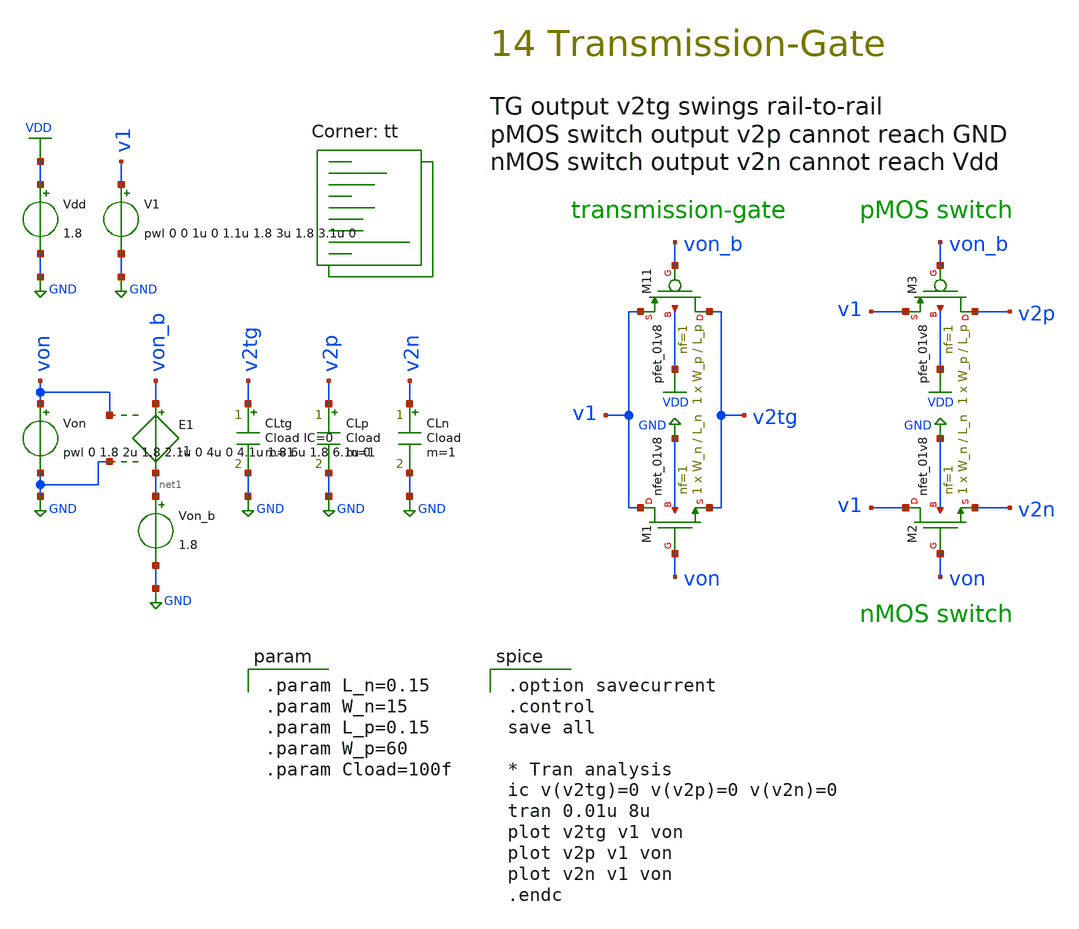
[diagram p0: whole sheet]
** sch_path: 14-b_transmission-gate_tran.sch
**.subckt 14-b_transmission-gate_tran
XM1 v1 von v2tg GND sky130_fd_pr__nfet_01v8 L=L_n W=W_n nf=1 ad='int((1 + 1)/2) * W_n / 1 * 0.29' as='int((1 + 2)/2) * W_n / 1 * 0.29'
+ pd='2*int((1 + 1)/2) * (W_n / 1 + 0.29)' ps='2*int((1 + 2)/2) * (W_n / 1 + 0.29)' nrd='0.29 / W_n ' nrs='0.29 / W_n '
+ sa=0 sb=0 sd=0 mult=1 m=1
V1 v1 GND pwl 0 0 1u 0 1.1u 1.8 3u 1.8 3.1u 0
Von von GND pwl 0 1.8 2u 1.8 2.1u 0 4u 0 4.1u 1.8 6u 1.8 6.1u 0
E1 von_b net1 von GND -1
Von_b net1 GND 1.8
XM11 v2tg von_b v1 VDD sky130_fd_pr__pfet_01v8 L=L_p W=W_p nf=1 ad='int((nf+1)/2) * W/nf * 0.29' as='int((nf+2)/2) * W/nf * 0.29'
+ pd='2*int((nf+1)/2) * (W/nf + 0.29)' ps='2*int((nf+2)/2) * (W/nf + 0.29)' nrd='0.29 / W' nrs='0.29 / W'
+ sa=0 sb=0 sd=0 mult=1 m=1
Vdd VDD GND 1.8
CLtg v2tg GND Cload IC=0 m=1
CLp v2p GND Cload m=1
CLn v2n GND Cload m=1
XM2 v1 von v2n GND sky130_fd_pr__nfet_01v8 L=L_n W=W_n nf=1 ad='int((1 + 1)/2) * W_n / 1 * 0.29' as='int((1 + 2)/2) * W_n / 1 * 0.29'
+ pd='2*int((1 + 1)/2) * (W_n / 1 + 0.29)' ps='2*int((1 + 2)/2) * (W_n / 1 + 0.29)' nrd='0.29 / W_n ' nrs='0.29 / W_n '
+ sa=0 sb=0 sd=0 mult=1 m=1
XM3 v2p von_b v1 VDD sky130_fd_pr__pfet_01v8 L=L_p W=W_p nf=1 ad='int((nf+1)/2) * W/nf * 0.29' as='int((nf+2)/2) * W/nf * 0.29'
+ pd='2*int((nf+1)/2) * (W/nf + 0.29)' ps='2*int((nf+2)/2) * (W/nf + 0.29)' nrd='0.29 / W' nrs='0.29 / W'
+ sa=0 sb=0 sd=0 mult=1 m=1
**** begin user architecture code
.lib $::SKYWATER_MODELS/sky130.lib.spice tt

.option savecurrent
.control
save all

* Tran analysis
ic v(v2tg)=0 v(v2p)=0 v(v2n)=0
tran 0.01u 8u
plot v2tg v1 von
plot v2p v1 von
plot v2n v1 von
.endc


.param L_n=0.15
.param W_n=15
.param L_p=0.15
.param W_p=60
.param Cload=100f

**** end user architecture code
**.ends
.GLOBAL GND
.GLOBAL VDD
.end
